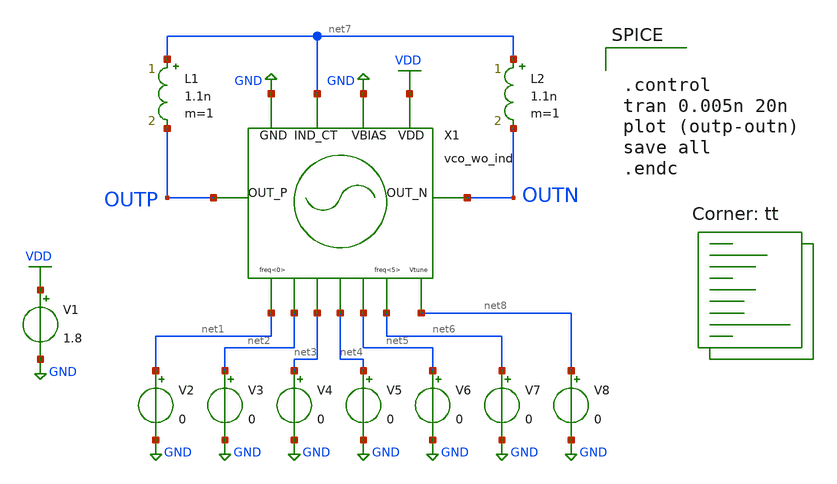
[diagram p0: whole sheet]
** sch_path: xschem/vco_wo_ind_tb.sch
**.subckt vco_wo_ind_tb
V1 VDD GND 1.8
V2 net1 GND 0
V3 net2 GND 0
V4 net3 GND 0
V5 net4 GND 0
V6 net5 GND 0
V7 net6 GND 0
L1 net7 OUTP 1.1n m=1
L2 net7 OUTN 1.1n m=1
X1 OUTP GND net7 VDD OUTN net1 net2 net3 net4 net5 net6 GND net8 vco_wo_ind
V8 net8 GND 0
**** begin user architecture code


.control
tran 0.005n 20n
plot (outp-outn)
save all
.endc


.lib $::SKYWATER_MODELS/sky130.lib.spice tt
**** end user architecture code
**.ends
.GLOBAL GND
.GLOBAL VDD
.end
